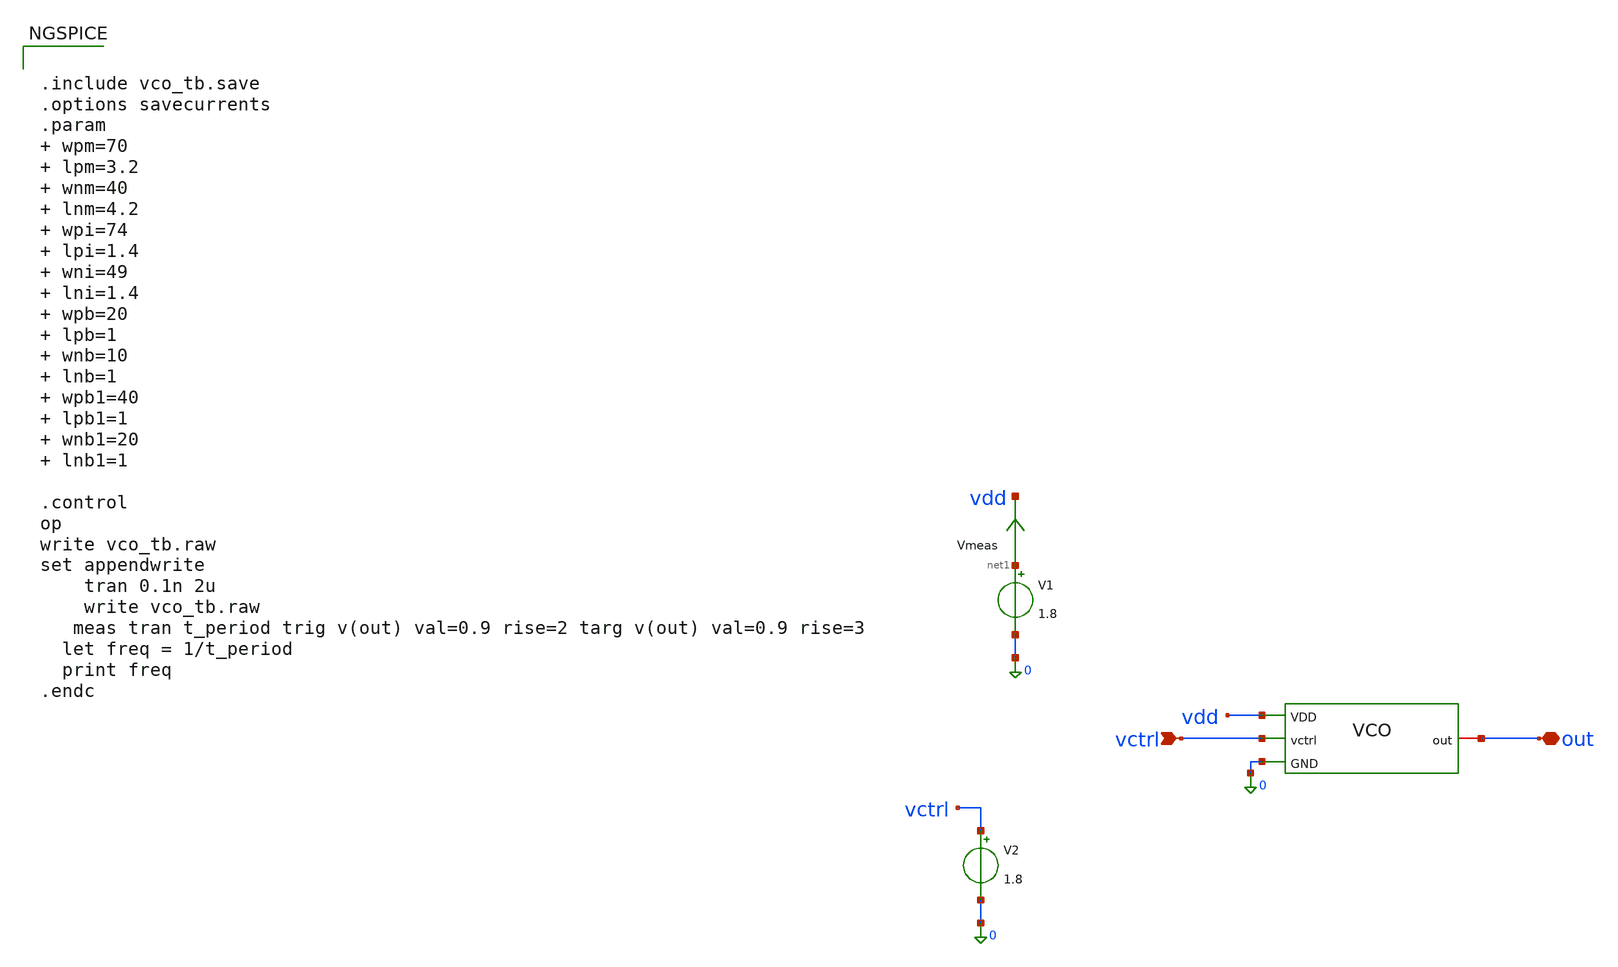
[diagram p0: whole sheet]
** sch_path: design_data/xschem/VCO/vco_tb.sch
**.subckt vco_tb vctrl out
*.ipin vctrl
*.iopin out
V1 net1 0 1.8
V2 vctrl 0 1.8
Vmeas net1 vdd 0
.save i(vmeas)
x1 vdd out vctrl 0 vco
**** begin user architecture code


.include vco_tb.save
.options savecurrents
.param  wpm=70  lpm=3.2  wnm=40  lnm=4.2  wpi=74  lpi=1.4  wni=49  lni=1.4  wpb=20  lpb=1  wnb=10
+  lnb=1  wpb1=40  lpb1=1  wnb1=20  lnb1=1

.control
op
write vco_tb.raw
set appendwrite
    tran 0.1n 2u
    write vco_tb.raw
   meas tran t_period trig v(out) val=0.9 rise=2 targ v(out) val=0.9 rise=3
  let freq = 1/t_period
  print freq
.endc



** opencircuitdesign pdks install
.lib $::SKYWATER_MODELS/sky130.lib.spice ff

**** end user architecture code
**.ends

* expanding   symbol:  xschem/VCO/vco.sym # of pins=4
** sym_path: xschem/VCO/vco.sym
** sch_path: xschem/VCO/vco.sch
.subckt vco VDD out vctrl GND
*.ipin vctrl
*.iopin out
*.ipin GND
*.ipin VDD
XM7 net5 net5 VDD VDD sky130_fd_pr__pfet_01v8 L=3.2 W=70 nf=1 ad='int((1 + 1)/2) * 70 / 1 * 0.29' as='int((1 + 2)/2) * 70 / 1 * 0.29'
+ pd='2*int((1 + 1)/2) * (70 / 1 + 0.29)' ps='2*int((1 + 2)/2) * (70 / 1 + 0.29)' nrd='0.29 / 70 ' nrs='0.29 / 70 '
+ sa=0 sb=0 sd=0 mult=1 m=1
XM8 net5 vctrl GND GND sky130_fd_pr__nfet_01v8 L=4.2 W=40 nf=1 ad='int((1 + 1)/2) * 40 / 1 * 0.29' as='int((1 + 2)/2) * 40 / 1 * 0.29'
+ pd='2*int((1 + 1)/2) * (40 / 1 + 0.29)' ps='2*int((1 + 2)/2) * (40 / 1 + 0.29)' nrd='0.29 / 40 ' nrs='0.29 / 40 '
+ sa=0 sb=0 sd=0 mult=1 m=1
XM5 net1 vctrl GND GND sky130_fd_pr__nfet_01v8 L=4.2 W=40 nf=1 ad='int((1 + 1)/2) * 40 / 1 * 0.29' as='int((1 + 2)/2) * 40 / 1 * 0.29'
+ pd='2*int((1 + 1)/2) * (40 / 1 + 0.29)' ps='2*int((1 + 2)/2) * (40 / 1 + 0.29)' nrd='0.29 / 40 ' nrs='0.29 / 40 '
+ sa=0 sb=0 sd=0 mult=1 m=1
XM6 net2 net4 net1 net1 sky130_fd_pr__nfet_01v8 L=1.4 W=49 nf=1 ad='int((1 + 1)/2) * 49 / 1 * 0.29' as='int((1 + 2)/2) * 49 / 1 * 0.29'
+ pd='2*int((1 + 1)/2) * (49 / 1 + 0.29)' ps='2*int((1 + 2)/2) * (49 / 1 + 0.29)' nrd='0.29 / 49 ' nrs='0.29 / 49 '
+ sa=0 sb=0 sd=0 mult=1 m=1
XM1 net3 net5 VDD VDD sky130_fd_pr__pfet_01v8 L=3.2 W=70 nf=1 ad='int((1 + 1)/2) * 70 / 1 * 0.29' as='int((1 + 2)/2) * 70 / 1 * 0.29'
+ pd='2*int((1 + 1)/2) * (70 / 1 + 0.29)' ps='2*int((1 + 2)/2) * (70 / 1 + 0.29)' nrd='0.29 / 70 ' nrs='0.29 / 70 '
+ sa=0 sb=0 sd=0 mult=1 m=1
XM2 net2 net4 net3 net3 sky130_fd_pr__pfet_01v8 L=1.4 W=74 nf=1 ad='int((1 + 1)/2) * 74 / 1 * 0.29' as='int((1 + 2)/2) * 74 / 1 * 0.29'
+ pd='2*int((1 + 1)/2) * (74 / 1 + 0.29)' ps='2*int((1 + 2)/2) * (74 / 1 + 0.29)' nrd='0.29 / 74 ' nrs='0.29 / 74 '
+ sa=0 sb=0 sd=0 mult=1 m=1
XM3 net6 vctrl GND GND sky130_fd_pr__nfet_01v8 L=4.2 W=40 nf=1 ad='int((1 + 1)/2) * 40 / 1 * 0.29' as='int((1 + 2)/2) * 40 / 1 * 0.29'
+ pd='2*int((1 + 1)/2) * (40 / 1 + 0.29)' ps='2*int((1 + 2)/2) * (40 / 1 + 0.29)' nrd='0.29 / 40 ' nrs='0.29 / 40 '
+ sa=0 sb=0 sd=0 mult=1 m=1
XM9 net7 net5 VDD VDD sky130_fd_pr__pfet_01v8 L=3.2 W=70 nf=1 ad='int((1 + 1)/2) * 70 / 1 * 0.29' as='int((1 + 2)/2) * 70 / 1 * 0.29'
+ pd='2*int((1 + 1)/2) * (70 / 1 + 0.29)' ps='2*int((1 + 2)/2) * (70 / 1 + 0.29)' nrd='0.29 / 70 ' nrs='0.29 / 70 '
+ sa=0 sb=0 sd=0 mult=1 m=1
XM11 net8 vctrl GND GND sky130_fd_pr__nfet_01v8 L=4.2 W=40 nf=1 ad='int((1 + 1)/2) * 40 / 1 * 0.29' as='int((1 + 2)/2) * 40 / 1 * 0.29'
+ pd='2*int((1 + 1)/2) * (40 / 1 + 0.29)' ps='2*int((1 + 2)/2) * (40 / 1 + 0.29)' nrd='0.29 / 40 ' nrs='0.29 / 40 '
+ sa=0 sb=0 sd=0 mult=1 m=1
XM13 net9 net5 VDD VDD sky130_fd_pr__pfet_01v8 L=3.2 W=70 nf=1 ad='int((1 + 1)/2) * 70 / 1 * 0.29' as='int((1 + 2)/2) * 70 / 1 * 0.29'
+ pd='2*int((1 + 1)/2) * (70 / 1 + 0.29)' ps='2*int((1 + 2)/2) * (70 / 1 + 0.29)' nrd='0.29 / 70 ' nrs='0.29 / 70 '
+ sa=0 sb=0 sd=0 mult=1 m=1
XM4 net10 net2 net6 net6 sky130_fd_pr__nfet_01v8 L=1.4 W=49 nf=1 ad='int((1 + 1)/2) * 49 / 1 * 0.29'
+ as='int((1 + 2)/2) * 49 / 1 * 0.29' pd='2*int((1 + 1)/2) * (49 / 1 + 0.29)' ps='2*int((1 + 2)/2) * (49 / 1 + 0.29)'
+ nrd='0.29 / 49 ' nrs='0.29 / 49 ' sa=0 sb=0 sd=0 mult=1 m=1
XM10 net10 net2 net7 net7 sky130_fd_pr__pfet_01v8 L=1.4 W=74 nf=1 ad='int((1 + 1)/2) * 74 / 1 * 0.29'
+ as='int((1 + 2)/2) * 74 / 1 * 0.29' pd='2*int((1 + 1)/2) * (74 / 1 + 0.29)' ps='2*int((1 + 2)/2) * (74 / 1 + 0.29)'
+ nrd='0.29 / 74 ' nrs='0.29 / 74 ' sa=0 sb=0 sd=0 mult=1 m=1
XM12 net4 net10 net8 net8 sky130_fd_pr__nfet_01v8 L=1.4 W=49 nf=1 ad='int((1 + 1)/2) * 49 / 1 * 0.29'
+ as='int((1 + 2)/2) * 49 / 1 * 0.29' pd='2*int((1 + 1)/2) * (49 / 1 + 0.29)' ps='2*int((1 + 2)/2) * (49 / 1 + 0.29)'
+ nrd='0.29 / 49 ' nrs='0.29 / 49 ' sa=0 sb=0 sd=0 mult=1 m=1
XM14 net4 net10 net9 net9 sky130_fd_pr__pfet_01v8 L=1.4 W=74 nf=1 ad='int((1 + 1)/2) * 74 / 1 * 0.29'
+ as='int((1 + 2)/2) * 74 / 1 * 0.29' pd='2*int((1 + 1)/2) * (74 / 1 + 0.29)' ps='2*int((1 + 2)/2) * (74 / 1 + 0.29)'
+ nrd='0.29 / 74 ' nrs='0.29 / 74 ' sa=0 sb=0 sd=0 mult=1 m=1
XM15 net11 net4 GND GND sky130_fd_pr__nfet_01v8 L=1 W=10 nf=1 ad='int((1 + 1)/2) * 10 / 1 * 0.29' as='int((1 + 2)/2) * 10 / 1 * 0.29'
+ pd='2*int((1 + 1)/2) * (10 / 1 + 0.29)' ps='2*int((1 + 2)/2) * (10 / 1 + 0.29)' nrd='0.29 / 10 ' nrs='0.29 / 10 '
+ sa=0 sb=0 sd=0 mult=1 m=1
XM16 net11 net4 VDD VDD sky130_fd_pr__pfet_01v8 L=1 W=20 nf=1 ad='int((1 + 1)/2) * 20 / 1 * 0.29' as='int((1 + 2)/2) * 20 / 1 * 0.29'
+ pd='2*int((1 + 1)/2) * (20 / 1 + 0.29)' ps='2*int((1 + 2)/2) * (20 / 1 + 0.29)' nrd='0.29 / 20 ' nrs='0.29 / 20 '
+ sa=0 sb=0 sd=0 mult=1 m=1
XM17 out net11 GND GND sky130_fd_pr__nfet_01v8 L=1 W=20 nf=1 ad='int((1 + 1)/2) * 20 / 1 * 0.29' as='int((1 + 2)/2) * 20 / 1 * 0.29'
+ pd='2*int((1 + 1)/2) * (20 / 1 + 0.29)' ps='2*int((1 + 2)/2) * (20 / 1 + 0.29)' nrd='0.29 / 20 ' nrs='0.29 / 20 '
+ sa=0 sb=0 sd=0 mult=1 m=1
XM18 out net11 VDD VDD sky130_fd_pr__pfet_01v8 L=1 W=40 nf=1 ad='int((1 + 1)/2) * 40 / 1 * 0.29' as='int((1 + 2)/2) * 40 / 1 * 0.29'
+ pd='2*int((1 + 1)/2) * (40 / 1 + 0.29)' ps='2*int((1 + 2)/2) * (40 / 1 + 0.29)' nrd='0.29 / 40 ' nrs='0.29 / 40 '
+ sa=0 sb=0 sd=0 mult=1 m=1
.ends

.end
